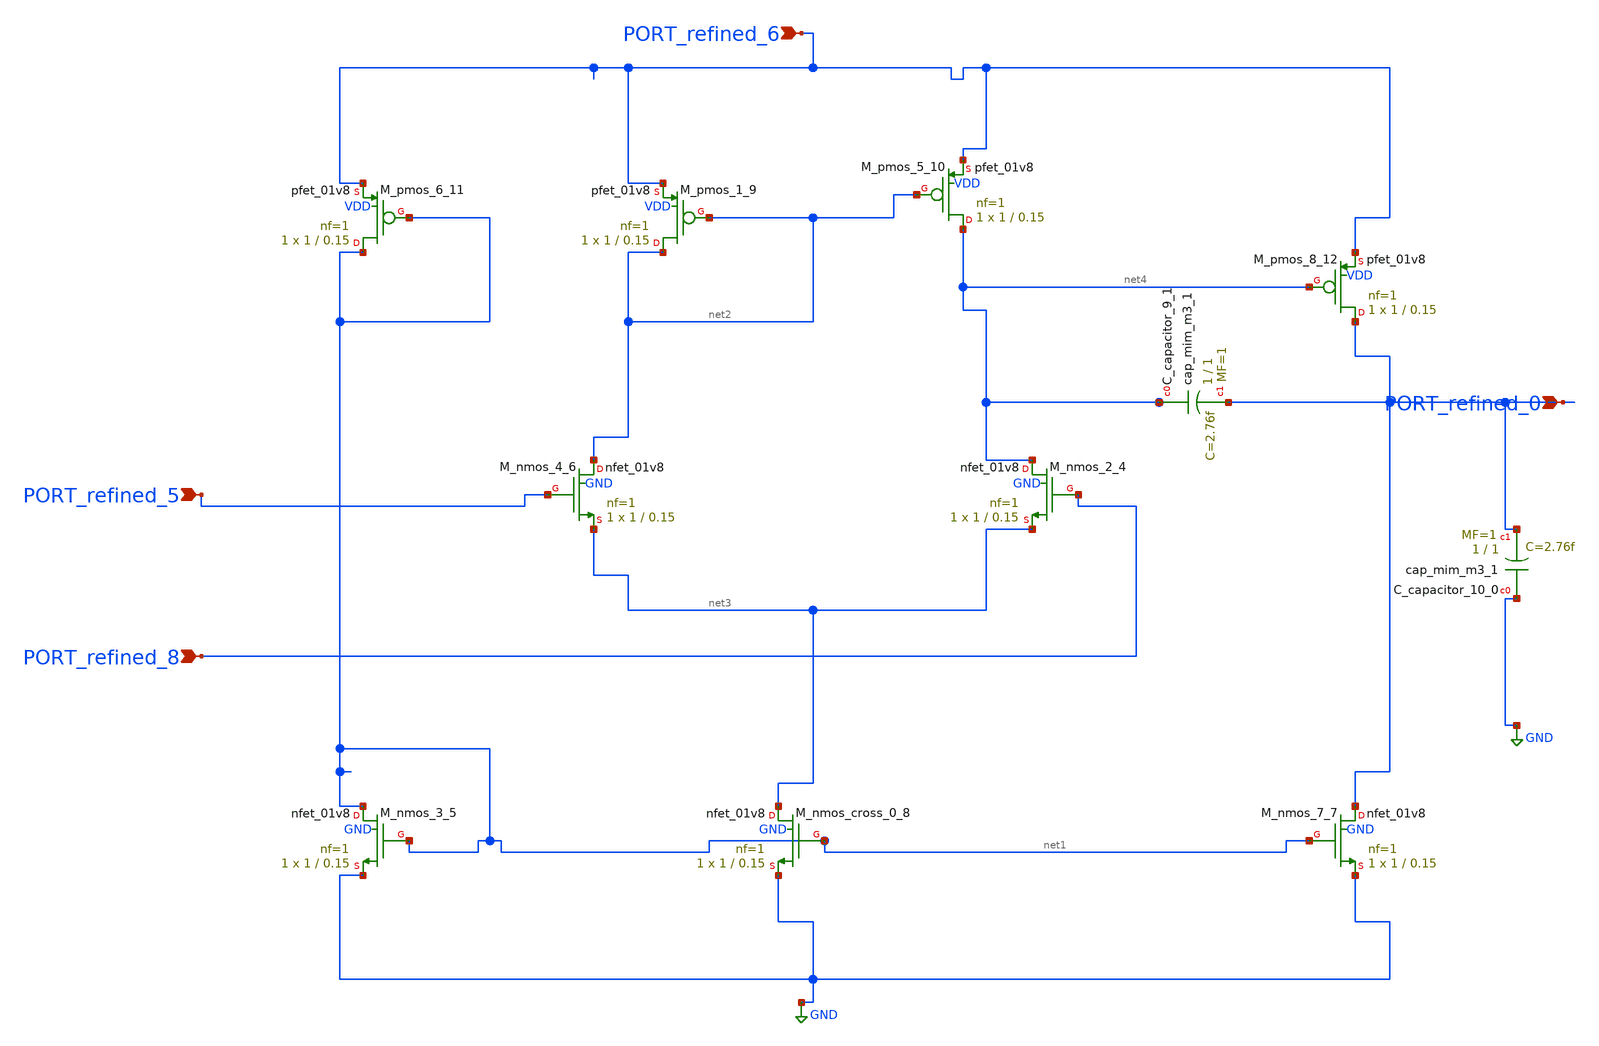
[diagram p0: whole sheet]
** sch_path: schematics/Image2Net/021.sch
**.subckt 021 PORT_refined_5 PORT_refined_8 PORT_refined_0 PORT_refined_6
*.ipin PORT_refined_5
*.ipin PORT_refined_8
*.ipin PORT_refined_0
*.ipin PORT_refined_6
XC_capacitor_10_0 GND PORT_refined_0 sky130_fd_pr__cap_mim_m3_1 W=1 L=1 MF=1 m=1
XC_capacitor_9_1 net4 PORT_refined_0 sky130_fd_pr__cap_mim_m3_1 W=1 L=1 MF=1 m=1
XM_nmos_2_4 net4 PORT_refined_8 net3 GND sky130_fd_pr__nfet_01v8 L=0.15 W=1 nf=1 ad='int((1 + 1)/2) * 1 / 1 * 0.29'
+ as='int((1 + 2)/2) * 1 / 1 * 0.29' pd='2*int((1 + 1)/2) * (1 / 1 + 0.29)' ps='2*int((1 + 2)/2) * (1 / 1 + 0.29)'
+ nrd='0.29 / 1 ' nrs='0.29 / 1 ' sa=0 sb=0 sd=0 mult=1 m=1
XM_nmos_3_5 net1 net1 GND GND sky130_fd_pr__nfet_01v8 L=0.15 W=1 nf=1 ad='int((1 + 1)/2) * 1 / 1 * 0.29'
+ as='int((1 + 2)/2) * 1 / 1 * 0.29' pd='2*int((1 + 1)/2) * (1 / 1 + 0.29)' ps='2*int((1 + 2)/2) * (1 / 1 + 0.29)'
+ nrd='0.29 / 1 ' nrs='0.29 / 1 ' sa=0 sb=0 sd=0 mult=1 m=1
XM_nmos_4_6 net2 PORT_refined_5 net3 GND sky130_fd_pr__nfet_01v8 L=0.15 W=1 nf=1 ad='int((1 + 1)/2) * 1 / 1 * 0.29'
+ as='int((1 + 2)/2) * 1 / 1 * 0.29' pd='2*int((1 + 1)/2) * (1 / 1 + 0.29)' ps='2*int((1 + 2)/2) * (1 / 1 + 0.29)'
+ nrd='0.29 / 1 ' nrs='0.29 / 1 ' sa=0 sb=0 sd=0 mult=1 m=1
XM_nmos_7_7 PORT_refined_0 net1 GND GND sky130_fd_pr__nfet_01v8 L=0.15 W=1 nf=1 ad='int((1 + 1)/2) * 1 / 1 * 0.29'
+ as='int((1 + 2)/2) * 1 / 1 * 0.29' pd='2*int((1 + 1)/2) * (1 / 1 + 0.29)' ps='2*int((1 + 2)/2) * (1 / 1 + 0.29)'
+ nrd='0.29 / 1 ' nrs='0.29 / 1 ' sa=0 sb=0 sd=0 mult=1 m=1
XM_nmos_cross_0_8 net3 net1 GND GND sky130_fd_pr__nfet_01v8 L=0.15 W=1 nf=1 ad='int((1 + 1)/2) * 1 / 1 * 0.29'
+ as='int((1 + 2)/2) * 1 / 1 * 0.29' pd='2*int((1 + 1)/2) * (1 / 1 + 0.29)' ps='2*int((1 + 2)/2) * (1 / 1 + 0.29)'
+ nrd='0.29 / 1 ' nrs='0.29 / 1 ' sa=0 sb=0 sd=0 mult=1 m=1
XM_pmos_1_9 net2 net2 PORT_refined_6 VDD sky130_fd_pr__pfet_01v8 L=0.15 W=1 nf=1 ad='int((1 + 1)/2) * 1 / 1 * 0.29'
+ as='int((1 + 2)/2) * 1 / 1 * 0.29' pd='2*int((1 + 1)/2) * (1 / 1 + 0.29)' ps='2*int((1 + 2)/2) * (1 / 1 + 0.29)'
+ nrd='0.29 / 1 ' nrs='0.29 / 1 ' sa=0 sb=0 sd=0 mult=1 m=1
XM_pmos_5_10 net4 net2 PORT_refined_6 VDD sky130_fd_pr__pfet_01v8 L=0.15 W=1 nf=1 ad='int((1 + 1)/2) * 1 / 1 * 0.29'
+ as='int((1 + 2)/2) * 1 / 1 * 0.29' pd='2*int((1 + 1)/2) * (1 / 1 + 0.29)' ps='2*int((1 + 2)/2) * (1 / 1 + 0.29)'
+ nrd='0.29 / 1 ' nrs='0.29 / 1 ' sa=0 sb=0 sd=0 mult=1 m=1
XM_pmos_6_11 net1 net1 PORT_refined_6 VDD sky130_fd_pr__pfet_01v8 L=0.15 W=1 nf=1 ad='int((1 + 1)/2) * 1 / 1 * 0.29'
+ as='int((1 + 2)/2) * 1 / 1 * 0.29' pd='2*int((1 + 1)/2) * (1 / 1 + 0.29)' ps='2*int((1 + 2)/2) * (1 / 1 + 0.29)'
+ nrd='0.29 / 1 ' nrs='0.29 / 1 ' sa=0 sb=0 sd=0 mult=1 m=1
XM_pmos_8_12 PORT_refined_0 net4 PORT_refined_6 VDD sky130_fd_pr__pfet_01v8 L=0.15 W=1 nf=1 ad='int((1 + 1)/2) * 1 / 1 * 0.29'
+ as='int((1 + 2)/2) * 1 / 1 * 0.29' pd='2*int((1 + 1)/2) * (1 / 1 + 0.29)' ps='2*int((1 + 2)/2) * (1 / 1 + 0.29)'
+ nrd='0.29 / 1 ' nrs='0.29 / 1 ' sa=0 sb=0 sd=0 mult=1 m=1
**.ends
.GLOBAL GND
.end
